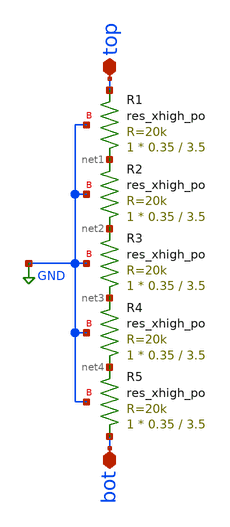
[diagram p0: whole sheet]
** sch_path: xschem/res100k.sch
**.subckt res100k top bot
*.iopin top
*.iopin bot
XR1 net1 top GND sky130_fd_pr__res_xhigh_po W=0.35 L=3.5 mult=1 m=1
XR2 net2 net1 GND sky130_fd_pr__res_xhigh_po W=0.35 L=3.5 mult=1 m=1
XR3 net3 net2 GND sky130_fd_pr__res_xhigh_po W=0.35 L=3.5 mult=1 m=1
XR4 net4 net3 GND sky130_fd_pr__res_xhigh_po W=0.35 L=3.5 mult=1 m=1
XR5 bot net4 GND sky130_fd_pr__res_xhigh_po W=0.35 L=3.5 mult=1 m=1
**.ends
.GLOBAL GND
.end
